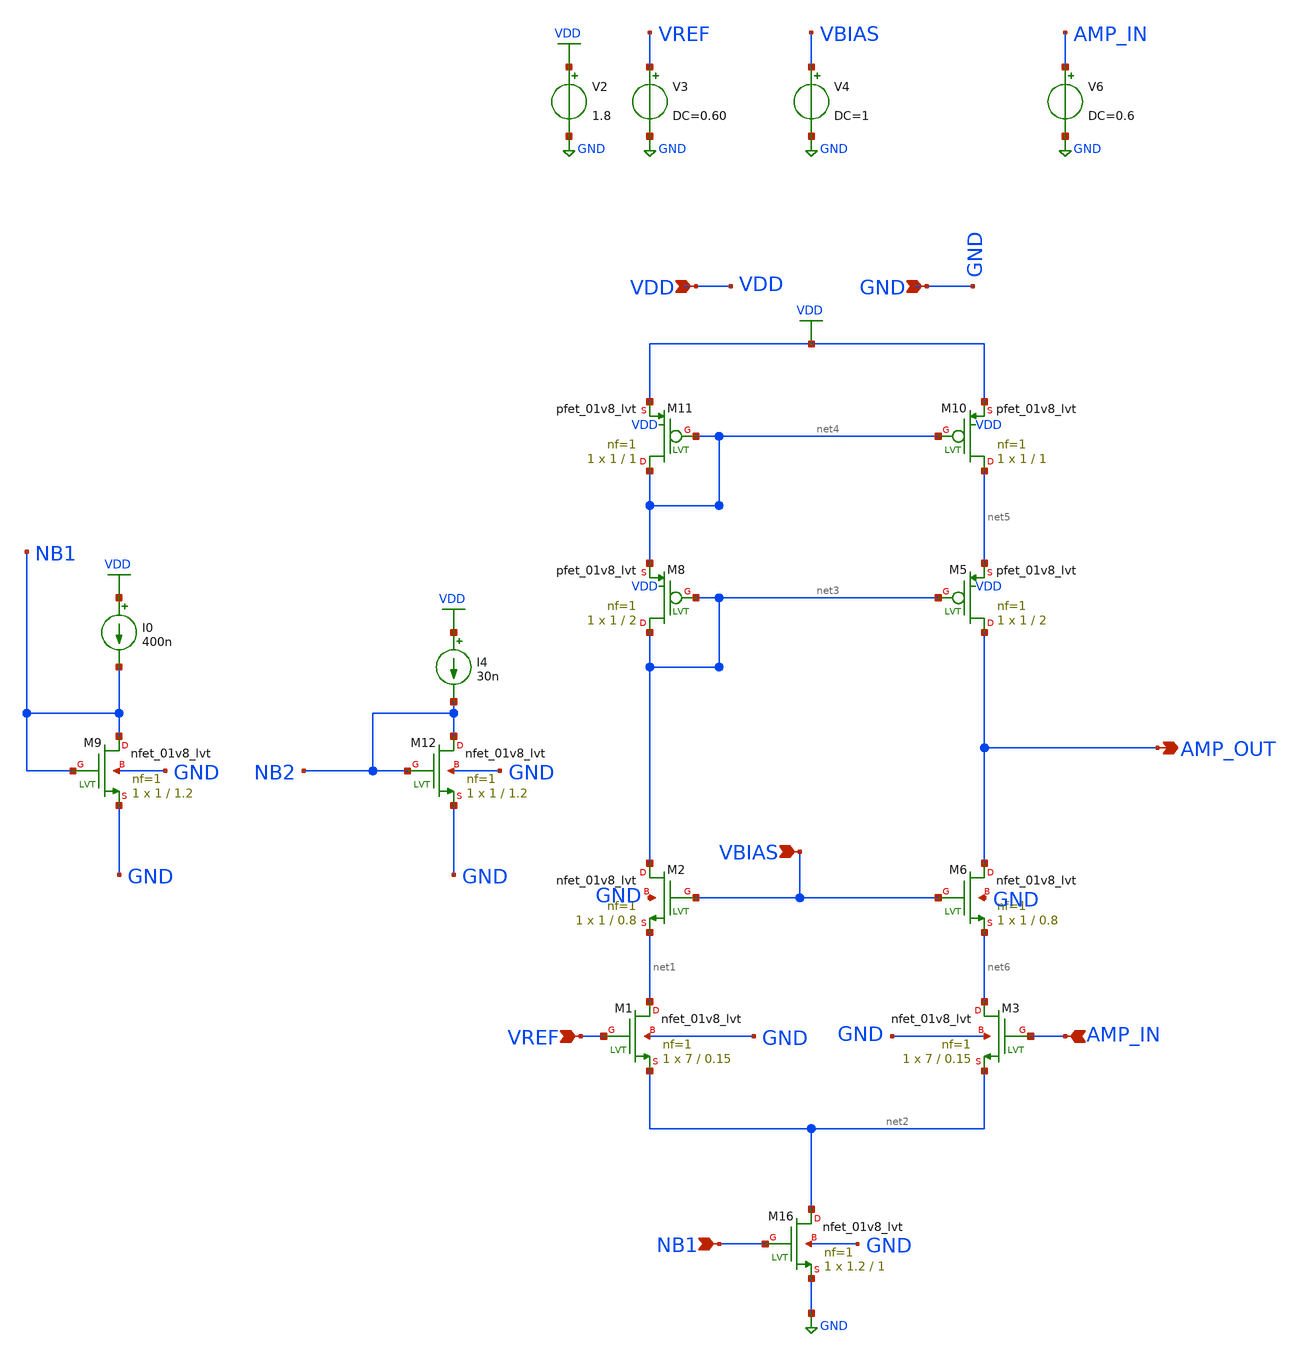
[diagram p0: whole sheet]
** sch_path: xschem/nmos_amp_simple.sch
**.subckt nmos_amp_simple VREF AMP_IN NB1 VBIAS VDD GND AMP_OUT
*.ipin VREF
*.ipin AMP_IN
*.ipin NB1
*.ipin VBIAS
*.ipin VDD
*.ipin GND
*.opin AMP_OUT
V2 VDD GND 1.8
V3 VREF GND DC=0.60
V4 VBIAS GND DC=1
XM8 net3 net3 net4 VDD sky130_fd_pr__pfet_01v8_lvt L=2 W=1 nf=1 ad='int((nf+1)/2) * W/nf * 0.29' as='int((nf+2)/2) * W/nf * 0.29'
+ pd='2*int((nf+1)/2) * (W/nf + 0.29)' ps='2*int((nf+2)/2) * (W/nf + 0.29)' nrd='0.29 / W' nrs='0.29 / W'
+ sa=0 sb=0 sd=0 mult=1 m=1
XM10 net5 net4 VDD VDD sky130_fd_pr__pfet_01v8_lvt L=1 W=1 nf=1 ad='int((nf+1)/2) * W/nf * 0.29' as='int((nf+2)/2) * W/nf * 0.29'
+ pd='2*int((nf+1)/2) * (W/nf + 0.29)' ps='2*int((nf+2)/2) * (W/nf + 0.29)' nrd='0.29 / W' nrs='0.29 / W'
+ sa=0 sb=0 sd=0 mult=1 m=1
XM11 net4 net4 VDD VDD sky130_fd_pr__pfet_01v8_lvt L=1 W=1 nf=1 ad='int((nf+1)/2) * W/nf * 0.29' as='int((nf+2)/2) * W/nf * 0.29'
+ pd='2*int((nf+1)/2) * (W/nf + 0.29)' ps='2*int((nf+2)/2) * (W/nf + 0.29)' nrd='0.29 / W' nrs='0.29 / W'
+ sa=0 sb=0 sd=0 mult=1 m=1
XM16 net2 NB1 GND GND sky130_fd_pr__nfet_01v8_lvt L=1 W=1.2 nf=1 ad='int((nf+1)/2) * W/nf * 0.29' as='int((nf+2)/2) * W/nf * 0.29'
+ pd='2*int((nf+1)/2) * (W/nf + 0.29)' ps='2*int((nf+2)/2) * (W/nf + 0.29)' nrd='0.29 / W' nrs='0.29 / W'
+ sa=0 sb=0 sd=0 mult=1 m=1
XM1 net1 VREF net2 GND sky130_fd_pr__nfet_01v8_lvt L=0.15 W=7 nf=1 ad='int((nf+1)/2) * W/nf * 0.29' as='int((nf+2)/2) * W/nf * 0.29'
+ pd='2*int((nf+1)/2) * (W/nf + 0.29)' ps='2*int((nf+2)/2) * (W/nf + 0.29)' nrd='0.29 / W' nrs='0.29 / W'
+ sa=0 sb=0 sd=0 mult=1 m=1
XM5 AMP_OUT net3 net5 VDD sky130_fd_pr__pfet_01v8_lvt L=2 W=1 nf=1 ad='int((nf+1)/2) * W/nf * 0.29' as='int((nf+2)/2) * W/nf * 0.29'
+ pd='2*int((nf+1)/2) * (W/nf + 0.29)' ps='2*int((nf+2)/2) * (W/nf + 0.29)' nrd='0.29 / W' nrs='0.29 / W'
+ sa=0 sb=0 sd=0 mult=1 m=1
XM2 net3 VBIAS net1 GND sky130_fd_pr__nfet_01v8_lvt L=0.8 W=1 nf=1 ad='int((nf+1)/2) * W/nf * 0.29' as='int((nf+2)/2) * W/nf * 0.29'
+ pd='2*int((nf+1)/2) * (W/nf + 0.29)' ps='2*int((nf+2)/2) * (W/nf + 0.29)' nrd='0.29 / W' nrs='0.29 / W'
+ sa=0 sb=0 sd=0 mult=1 m=1
XM3 net6 AMP_IN net2 GND sky130_fd_pr__nfet_01v8_lvt L=0.15 W=7 nf=1 ad='int((nf+1)/2) * W/nf * 0.29'
+ as='int((nf+2)/2) * W/nf * 0.29' pd='2*int((nf+1)/2) * (W/nf + 0.29)' ps='2*int((nf+2)/2) * (W/nf + 0.29)'
+ nrd='0.29 / W' nrs='0.29 / W' sa=0 sb=0 sd=0 mult=1 m=1
XM6 AMP_OUT VBIAS net6 GND sky130_fd_pr__nfet_01v8_lvt L=0.8 W=1 nf=1 ad='int((nf+1)/2) * W/nf * 0.29'
+ as='int((nf+2)/2) * W/nf * 0.29' pd='2*int((nf+1)/2) * (W/nf + 0.29)' ps='2*int((nf+2)/2) * (W/nf + 0.29)'
+ nrd='0.29 / W' nrs='0.29 / W' sa=0 sb=0 sd=0 mult=1 m=1
XM9 NB1 NB1 GND GND sky130_fd_pr__nfet_01v8_lvt L=1.2 W=1 nf=1 ad='int((nf+1)/2) * W/nf * 0.29' as='int((nf+2)/2) * W/nf * 0.29'
+ pd='2*int((nf+1)/2) * (W/nf + 0.29)' ps='2*int((nf+2)/2) * (W/nf + 0.29)' nrd='0.29 / W' nrs='0.29 / W'
+ sa=0 sb=0 sd=0 mult=1 m=1
I0 VDD NB1 400n
I4 VDD NB2 30n
XM12 NB2 NB2 GND GND sky130_fd_pr__nfet_01v8_lvt L=1.2 W=1 nf=1 ad='int((nf+1)/2) * W/nf * 0.29' as='int((nf+2)/2) * W/nf * 0.29'
+ pd='2*int((nf+1)/2) * (W/nf + 0.29)' ps='2*int((nf+2)/2) * (W/nf + 0.29)' nrd='0.29 / W' nrs='0.29 / W'
+ sa=0 sb=0 sd=0 mult=1 m=1
V6 AMP_IN GND DC=0.6
**** begin user architecture code

** opencircuitdesign pdks install
.lib $::SKYWATER_MODELS/sky130.lib.spice tt


**** end user architecture code
**.ends
.GLOBAL GND
.GLOBAL VDD
**** begin user architecture code


.options gmin=0.0000000000000000000001
*.options savecurrents

.control
save all

*tran 1m 50m
*plot v(test)
DC V5 0.2 0.8 0.001
plot v(amp_out)

*noise v(PIX_OUT) V8 dec 10 1 1Meg
*setplot noise2
*print onoise_total

*noise v(PIX_OUT) V8 dec 10 1 1Meg
*setplot noise2
*print onoise_total
.endc


**** end user architecture code
.end
